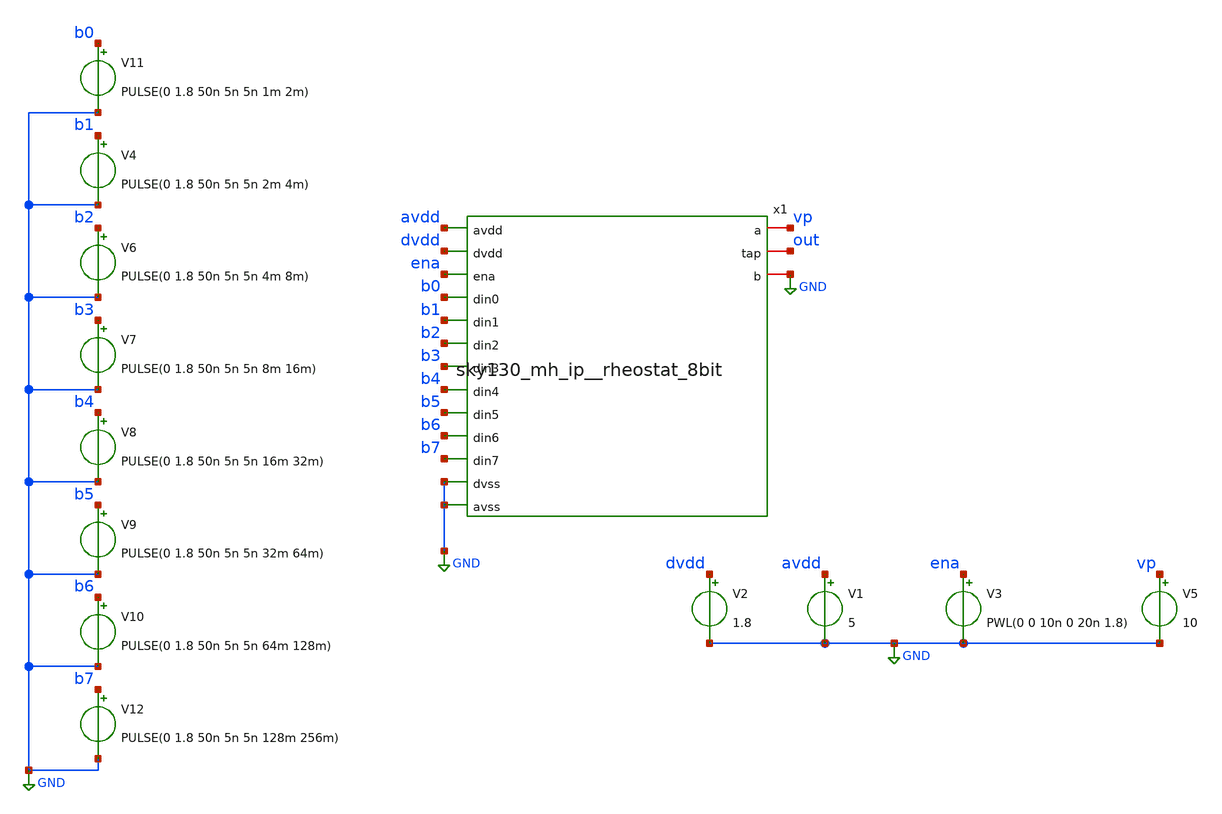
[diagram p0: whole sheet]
** sch_path: xschem/8bit_rheostat_tb.sch
**.subckt 8bit_rheostat_tb
V11 b0 GND PULSE(0 1.8 50n 5n 5n 1m 2m)
V4 b1 GND PULSE(0 1.8 50n 5n 5n 2m 4m)
V6 b2 GND PULSE(0 1.8 50n 5n 5n 4m 8m)
V7 b3 GND PULSE(0 1.8 50n 5n 5n 8m 16m)
V8 b4 GND PULSE(0 1.8 50n 5n 5n 16m 32m)
V9 b5 GND PULSE(0 1.8 50n 5n 5n 32m 64m)
V10 b6 GND PULSE(0 1.8 50n 5n 5n 64m 128m)
V12 b7 GND PULSE(0 1.8 50n 5n 5n 128m 256m)
V1 avdd GND 5
V3 ena GND PWL(0 0 10n 0 20n 1.8)
V5 vp GND 10
x1 avdd dvdd ena b0 vp b1 b2 out b3 GND b4 b5 b6 b7 GND GND sky130_mh_ip__rheostat_8bit
V2 dvdd GND 1.8
**** begin user architecture code


.option wnflag=0
.option savecurrents
.control
tran 1m 60m
plot V(out)
.endc

 .lib $::SKYWATER_MODELS/sky130.lib.spice tt
.include $::SKYWATER_STDCELLS/../../sky130_fd_sc_hvl/spice/sky130_fd_sc_hvl.spice

.param mc_mm_switch=0
.param mc_pr_switch=1

**** end user architecture code
**.ends

* expanding   symbol:  sky130_mh_ip__rheostat_8bit.sym # of pins=16
** sym_path: xschem/sky130_mh_ip__rheostat_8bit.sym
** sch_path: xschem/sky130_mh_ip__rheostat_8bit.sch
.subckt sky130_mh_ip__rheostat_8bit avdd dvdd ena din0 a din1 din2 tap din3 b din4 din5 din6 din7
+ dvss avss
*.ipin din0
*.ipin din1
*.ipin din2
*.ipin din3
*.ipin din4
*.ipin din5
*.ipin din6
*.ipin din7
*.iopin a
*.iopin tap
*.iopin b
*.ipin dvss
*.ipin avdd
*.ipin avss
*.ipin ena
*.ipin dvdd
x1 avdd nb0 nb5 nb6 nb3 nb4 nb1 nb7 nb2 a tap pb3 pb2 pb4 pb1 pb5 pb7 pb6 pb0 avss
+ 8bit_half_rheostat
x2 avdd dvdd nb0 ena pb0 din0 dvss avss double_output_buffer
x3 avdd dvdd nb1 ena pb1 din1 dvss avss double_output_buffer
x4 avdd dvdd nb2 ena pb2 din2 dvss avss double_output_buffer
x5 avdd dvdd nb3 ena pb3 din3 dvss avss double_output_buffer
x6 avdd dvdd nb4 ena pb4 din4 dvss avss double_output_buffer
x7 avdd dvdd nb5 ena pb5 din5 dvss avss double_output_buffer
x8 avdd dvdd nb6 ena pb6 din6 dvss avss double_output_buffer
x9 avdd dvdd nb7 ena pb7 din7 dvss avss double_output_buffer
x10 avdd pb0 pb5 pb6 pb3 pb4 pb1 pb7 pb2 tap b nb3 nb2 nb4 nb1 nb5 nb7 nb6 nb0 avss
+ 8bit_half_rheostat
.ends


* expanding   symbol:  8bit_half_rheostat.sym # of pins=20
** sym_path: xschem/8bit_half_rheostat.sym
** sch_path: xschem/8bit_half_rheostat.sch
.subckt 8bit_half_rheostat avdd inn0 inn5 inn6 inn3 inn4 inn1 inn7 inn2 a b inp3 inp2 inp4 inp1 inp5
+ inp7 inp6 inp0 avss
*.iopin b
*.iopin a
*.ipin inn0
*.ipin inn1
*.ipin inn2
*.ipin inn3
*.ipin inn4
*.ipin inn5
*.ipin inn6
*.ipin inn7
*.ipin inp0
*.ipin inp1
*.ipin inp2
*.ipin inp3
*.ipin inp4
*.ipin inp5
*.ipin inp6
*.ipin inp7
*.ipin avdd
*.ipin avss
XM17 a inn0 net1 avdd sky130_fd_pr__pfet_g5v0d10v5 L=10 W=0.5 nf=1 ad='int((nf+1)/2) * W/nf * 0.29' as='int((nf+2)/2) * W/nf * 0.29'
+ pd='2*int((nf+1)/2) * (W/nf + 0.29)' ps='2*int((nf+2)/2) * (W/nf + 0.29)' nrd='0.29 / W' nrs='0.29 / W'
+ sa=0 sb=0 sd=0 mult=1 m=1
XM18 a inp0 net1 avss sky130_fd_pr__nfet_g5v0d10v5 L=0.5 W=10 nf=1 ad='int((nf+1)/2) * W/nf * 0.29' as='int((nf+2)/2) * W/nf * 0.29'
+ pd='2*int((nf+1)/2) * (W/nf + 0.29)' ps='2*int((nf+2)/2) * (W/nf + 0.29)' nrd='0.29 / W' nrs='0.29 / W'
+ sa=0 sb=0 sd=0 mult=1 m=1
XM19 net1 inn1 net2 avdd sky130_fd_pr__pfet_g5v0d10v5 L=10 W=0.5 nf=1 ad='int((nf+1)/2) * W/nf * 0.29'
+ as='int((nf+2)/2) * W/nf * 0.29' pd='2*int((nf+1)/2) * (W/nf + 0.29)' ps='2*int((nf+2)/2) * (W/nf + 0.29)'
+ nrd='0.29 / W' nrs='0.29 / W' sa=0 sb=0 sd=0 mult=1 m=1
XM20 net1 inp1 net2 avss sky130_fd_pr__nfet_g5v0d10v5 L=0.5 W=10 nf=1 ad='int((nf+1)/2) * W/nf * 0.29'
+ as='int((nf+2)/2) * W/nf * 0.29' pd='2*int((nf+1)/2) * (W/nf + 0.29)' ps='2*int((nf+2)/2) * (W/nf + 0.29)'
+ nrd='0.29 / W' nrs='0.29 / W' sa=0 sb=0 sd=0 mult=1 m=1
XM21 net2 inn2 net3 avdd sky130_fd_pr__pfet_g5v0d10v5 L=10 W=0.5 nf=1 ad='int((nf+1)/2) * W/nf * 0.29'
+ as='int((nf+2)/2) * W/nf * 0.29' pd='2*int((nf+1)/2) * (W/nf + 0.29)' ps='2*int((nf+2)/2) * (W/nf + 0.29)'
+ nrd='0.29 / W' nrs='0.29 / W' sa=0 sb=0 sd=0 mult=1 m=1
XM22 net2 inp2 net3 avss sky130_fd_pr__nfet_g5v0d10v5 L=0.5 W=10 nf=1 ad='int((nf+1)/2) * W/nf * 0.29'
+ as='int((nf+2)/2) * W/nf * 0.29' pd='2*int((nf+1)/2) * (W/nf + 0.29)' ps='2*int((nf+2)/2) * (W/nf + 0.29)'
+ nrd='0.29 / W' nrs='0.29 / W' sa=0 sb=0 sd=0 mult=1 m=1
XM23 net3 inn3 net4 avdd sky130_fd_pr__pfet_g5v0d10v5 L=10 W=0.5 nf=1 ad='int((nf+1)/2) * W/nf * 0.29'
+ as='int((nf+2)/2) * W/nf * 0.29' pd='2*int((nf+1)/2) * (W/nf + 0.29)' ps='2*int((nf+2)/2) * (W/nf + 0.29)'
+ nrd='0.29 / W' nrs='0.29 / W' sa=0 sb=0 sd=0 mult=1 m=1
XM24 net3 inp3 net4 avss sky130_fd_pr__nfet_g5v0d10v5 L=0.5 W=10 nf=1 ad='int((nf+1)/2) * W/nf * 0.29'
+ as='int((nf+2)/2) * W/nf * 0.29' pd='2*int((nf+1)/2) * (W/nf + 0.29)' ps='2*int((nf+2)/2) * (W/nf + 0.29)'
+ nrd='0.29 / W' nrs='0.29 / W' sa=0 sb=0 sd=0 mult=1 m=1
XM25 net4 inn4 net5 avdd sky130_fd_pr__pfet_g5v0d10v5 L=10 W=0.5 nf=1 ad='int((nf+1)/2) * W/nf * 0.29'
+ as='int((nf+2)/2) * W/nf * 0.29' pd='2*int((nf+1)/2) * (W/nf + 0.29)' ps='2*int((nf+2)/2) * (W/nf + 0.29)'
+ nrd='0.29 / W' nrs='0.29 / W' sa=0 sb=0 sd=0 mult=1 m=1
XM26 net4 inp4 net5 avss sky130_fd_pr__nfet_g5v0d10v5 L=0.5 W=10 nf=1 ad='int((nf+1)/2) * W/nf * 0.29'
+ as='int((nf+2)/2) * W/nf * 0.29' pd='2*int((nf+1)/2) * (W/nf + 0.29)' ps='2*int((nf+2)/2) * (W/nf + 0.29)'
+ nrd='0.29 / W' nrs='0.29 / W' sa=0 sb=0 sd=0 mult=1 m=1
XM27 net5 inn5 net6 avdd sky130_fd_pr__pfet_g5v0d10v5 L=10 W=0.5 nf=1 ad='int((nf+1)/2) * W/nf * 0.29'
+ as='int((nf+2)/2) * W/nf * 0.29' pd='2*int((nf+1)/2) * (W/nf + 0.29)' ps='2*int((nf+2)/2) * (W/nf + 0.29)'
+ nrd='0.29 / W' nrs='0.29 / W' sa=0 sb=0 sd=0 mult=1 m=1
XM28 net5 inp5 net6 avss sky130_fd_pr__nfet_g5v0d10v5 L=0.5 W=10 nf=1 ad='int((nf+1)/2) * W/nf * 0.29'
+ as='int((nf+2)/2) * W/nf * 0.29' pd='2*int((nf+1)/2) * (W/nf + 0.29)' ps='2*int((nf+2)/2) * (W/nf + 0.29)'
+ nrd='0.29 / W' nrs='0.29 / W' sa=0 sb=0 sd=0 mult=1 m=1
XM29 net6 inn6 net7 avdd sky130_fd_pr__pfet_g5v0d10v5 L=10 W=0.5 nf=1 ad='int((nf+1)/2) * W/nf * 0.29'
+ as='int((nf+2)/2) * W/nf * 0.29' pd='2*int((nf+1)/2) * (W/nf + 0.29)' ps='2*int((nf+2)/2) * (W/nf + 0.29)'
+ nrd='0.29 / W' nrs='0.29 / W' sa=0 sb=0 sd=0 mult=1 m=1
XM30 net6 inp6 net7 avss sky130_fd_pr__nfet_g5v0d10v5 L=0.5 W=10 nf=1 ad='int((nf+1)/2) * W/nf * 0.29'
+ as='int((nf+2)/2) * W/nf * 0.29' pd='2*int((nf+1)/2) * (W/nf + 0.29)' ps='2*int((nf+2)/2) * (W/nf + 0.29)'
+ nrd='0.29 / W' nrs='0.29 / W' sa=0 sb=0 sd=0 mult=1 m=1
XM31 net7 inn7 b avdd sky130_fd_pr__pfet_g5v0d10v5 L=10 W=0.5 nf=1 ad='int((nf+1)/2) * W/nf * 0.29' as='int((nf+2)/2) * W/nf * 0.29'
+ pd='2*int((nf+1)/2) * (W/nf + 0.29)' ps='2*int((nf+2)/2) * (W/nf + 0.29)' nrd='0.29 / W' nrs='0.29 / W'
+ sa=0 sb=0 sd=0 mult=1 m=1
XM32 net7 inp7 b avss sky130_fd_pr__nfet_g5v0d10v5 L=0.5 W=10 nf=1 ad='int((nf+1)/2) * W/nf * 0.29' as='int((nf+2)/2) * W/nf * 0.29'
+ pd='2*int((nf+1)/2) * (W/nf + 0.29)' ps='2*int((nf+2)/2) * (W/nf + 0.29)' nrd='0.29 / W' nrs='0.29 / W'
+ sa=0 sb=0 sd=0 mult=1 m=1
XR9 a net1 sky130_fd_pr__res_generic_po W=0.957 L=2 m=1
XR10 net1 net2 sky130_fd_pr__res_generic_po W=0.957 L=4 m=1
XR11 net2 net3 sky130_fd_pr__res_generic_po W=0.957 L=8 m=1
XR12 net3 net4 sky130_fd_pr__res_generic_po W=0.957 L=16 m=1
XR13 net4 net5 sky130_fd_pr__res_generic_po W=0.957 L=32 m=1
XR14 net5 net6 sky130_fd_pr__res_generic_po W=0.957 L=64 m=1
XR15 net6 net7 sky130_fd_pr__res_generic_po W=0.957 L=128 m=1
XR16 net7 b sky130_fd_pr__res_generic_po W=0.957 L=256 m=1
.ends


* expanding   symbol:  double_output_buffer.sym # of pins=8
** sym_path: xschem/double_output_buffer.sym
** sch_path: xschem/double_output_buffer.sch
.subckt double_output_buffer avdd dvdd nout en pout din dvss avss
*.ipin din
*.ipin dvdd
*.ipin dvss
*.opin pout
*.opin nout
*.ipin en
*.ipin avdd
*.ipin avss
XM1 net1 en dvdd dvdd sky130_fd_pr__pfet_01v8 L=0.15 W=1 nf=1 ad='int((nf+1)/2) * W/nf * 0.29' as='int((nf+2)/2) * W/nf * 0.29'
+ pd='2*int((nf+1)/2) * (W/nf + 0.29)' ps='2*int((nf+2)/2) * (W/nf + 0.29)' nrd='0.29 / W' nrs='0.29 / W'
+ sa=0 sb=0 sd=0 mult=1 m=1
XM2 net1 din dvdd dvdd sky130_fd_pr__pfet_01v8 L=0.15 W=1 nf=1 ad='int((nf+1)/2) * W/nf * 0.29' as='int((nf+2)/2) * W/nf * 0.29'
+ pd='2*int((nf+1)/2) * (W/nf + 0.29)' ps='2*int((nf+2)/2) * (W/nf + 0.29)' nrd='0.29 / W' nrs='0.29 / W'
+ sa=0 sb=0 sd=0 mult=1 m=1
XM3 net3 net1 dvdd dvdd sky130_fd_pr__pfet_01v8 L=0.15 W=1 nf=1 ad='int((nf+1)/2) * W/nf * 0.29' as='int((nf+2)/2) * W/nf * 0.29'
+ pd='2*int((nf+1)/2) * (W/nf + 0.29)' ps='2*int((nf+2)/2) * (W/nf + 0.29)' nrd='0.29 / W' nrs='0.29 / W'
+ sa=0 sb=0 sd=0 mult=1 m=1
XM4 net1 en net2 dvss sky130_fd_pr__nfet_01v8 L=0.15 W=1 nf=1 ad='int((nf+1)/2) * W/nf * 0.29' as='int((nf+2)/2) * W/nf * 0.29'
+ pd='2*int((nf+1)/2) * (W/nf + 0.29)' ps='2*int((nf+2)/2) * (W/nf + 0.29)' nrd='0.29 / W' nrs='0.29 / W'
+ sa=0 sb=0 sd=0 mult=1 m=1
XM5 net2 din dvss dvss sky130_fd_pr__nfet_01v8 L=0.15 W=1 nf=1 ad='int((nf+1)/2) * W/nf * 0.29' as='int((nf+2)/2) * W/nf * 0.29'
+ pd='2*int((nf+1)/2) * (W/nf + 0.29)' ps='2*int((nf+2)/2) * (W/nf + 0.29)' nrd='0.29 / W' nrs='0.29 / W'
+ sa=0 sb=0 sd=0 mult=1 m=1
XM6 net3 net1 dvss dvss sky130_fd_pr__nfet_01v8 L=0.15 W=1 nf=1 ad='int((nf+1)/2) * W/nf * 0.29' as='int((nf+2)/2) * W/nf * 0.29'
+ pd='2*int((nf+1)/2) * (W/nf + 0.29)' ps='2*int((nf+2)/2) * (W/nf + 0.29)' nrd='0.29 / W' nrs='0.29 / W'
+ sa=0 sb=0 sd=0 mult=1 m=1
XM7 nout net3 avdd avdd sky130_fd_pr__pfet_g5v0d10v5 L=1 W=2 nf=1 ad='int((nf+1)/2) * W/nf * 0.29' as='int((nf+2)/2) * W/nf * 0.29'
+ pd='2*int((nf+1)/2) * (W/nf + 0.29)' ps='2*int((nf+2)/2) * (W/nf + 0.29)' nrd='0.29 / W' nrs='0.29 / W'
+ sa=0 sb=0 sd=0 mult=1 m=1
XM8 nout net3 avss avss sky130_fd_pr__nfet_g5v0d10v5 L=1 W=2 nf=1 ad='int((nf+1)/2) * W/nf * 0.29' as='int((nf+2)/2) * W/nf * 0.29'
+ pd='2*int((nf+1)/2) * (W/nf + 0.29)' ps='2*int((nf+2)/2) * (W/nf + 0.29)' nrd='0.29 / W' nrs='0.29 / W'
+ sa=0 sb=0 sd=0 mult=1 m=1
XM9 pout nout avdd avdd sky130_fd_pr__pfet_g5v0d10v5 L=1 W=2 nf=1 ad='int((nf+1)/2) * W/nf * 0.29' as='int((nf+2)/2) * W/nf * 0.29'
+ pd='2*int((nf+1)/2) * (W/nf + 0.29)' ps='2*int((nf+2)/2) * (W/nf + 0.29)' nrd='0.29 / W' nrs='0.29 / W'
+ sa=0 sb=0 sd=0 mult=1 m=1
XM10 pout nout net4 net4 sky130_fd_pr__nfet_g5v0d10v5 L=1 W=2 nf=1 ad='int((nf+1)/2) * W/nf * 0.29' as='int((nf+2)/2) * W/nf * 0.29'
+ pd='2*int((nf+1)/2) * (W/nf + 0.29)' ps='2*int((nf+2)/2) * (W/nf + 0.29)' nrd='0.29 / W' nrs='0.29 / W'
+ sa=0 sb=0 sd=0 mult=1 m=1
.ends

.GLOBAL GND
.end
